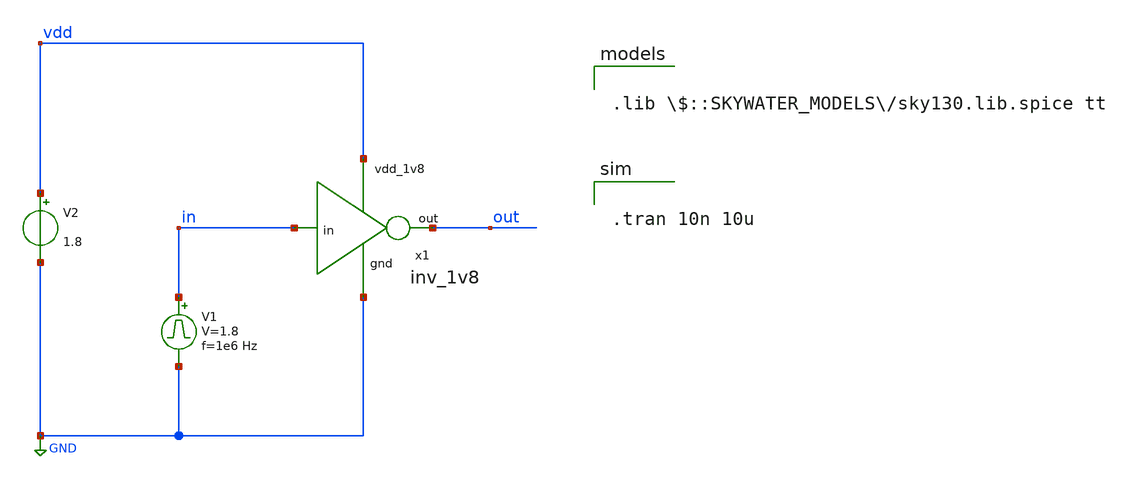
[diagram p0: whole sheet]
** sch_path: design/inv_1v8/test/inv_1v8_tb.sch
**.subckt inv_1v8_tb
V1 in GND pulse 0 1.8 '0.495/ 1e6 ' '0.01/1e6 ' '0.01/1e6 ' '0.49/1e6 ' '1/1e6 '
V2 vdd GND 1.8
x1 vdd in out GND inv_1v8
**** begin user architecture code


.tran 10n 10u



.lib $::SKYWATER_MODELS/sky130.lib.spice tt

**** end user architecture code
**.ends

* expanding   symbol:  inv_1v8/inv_1v8.sym # of pins=4
** sym_path: design/inv_1v8/inv_1v8.sym
** sch_path: design/inv_1v8/inv_1v8.sch
.subckt inv_1v8 vdd_1v8 in out gnd
*.ipin vdd_1v8
*.ipin gnd
*.ipin in
*.opin out
XM1 out in gnd gnd sky130_fd_pr__nfet_01v8 L=0.15 W=1 nf=1 ad='int((nf+1)/2) * W/nf * 0.29' as='int((nf+2)/2) * W/nf * 0.29'
+ pd='2*int((nf+1)/2) * (W/nf + 0.29)' ps='2*int((nf+2)/2) * (W/nf + 0.29)' nrd='0.29 / W' nrs='0.29 / W'
+ sa=0 sb=0 sd=0 mult=1 m=1
XM2 out in vdd_1v8 vdd_1v8 sky130_fd_pr__pfet_01v8 L=0.15 W=1 nf=1 ad='int((nf+1)/2) * W/nf * 0.29' as='int((nf+2)/2) * W/nf * 0.29'
+ pd='2*int((nf+1)/2) * (W/nf + 0.29)' ps='2*int((nf+2)/2) * (W/nf + 0.29)' nrd='0.29 / W' nrs='0.29 / W'
+ sa=0 sb=0 sd=0 mult=1 m=1
.ends

.GLOBAL GND
.end
